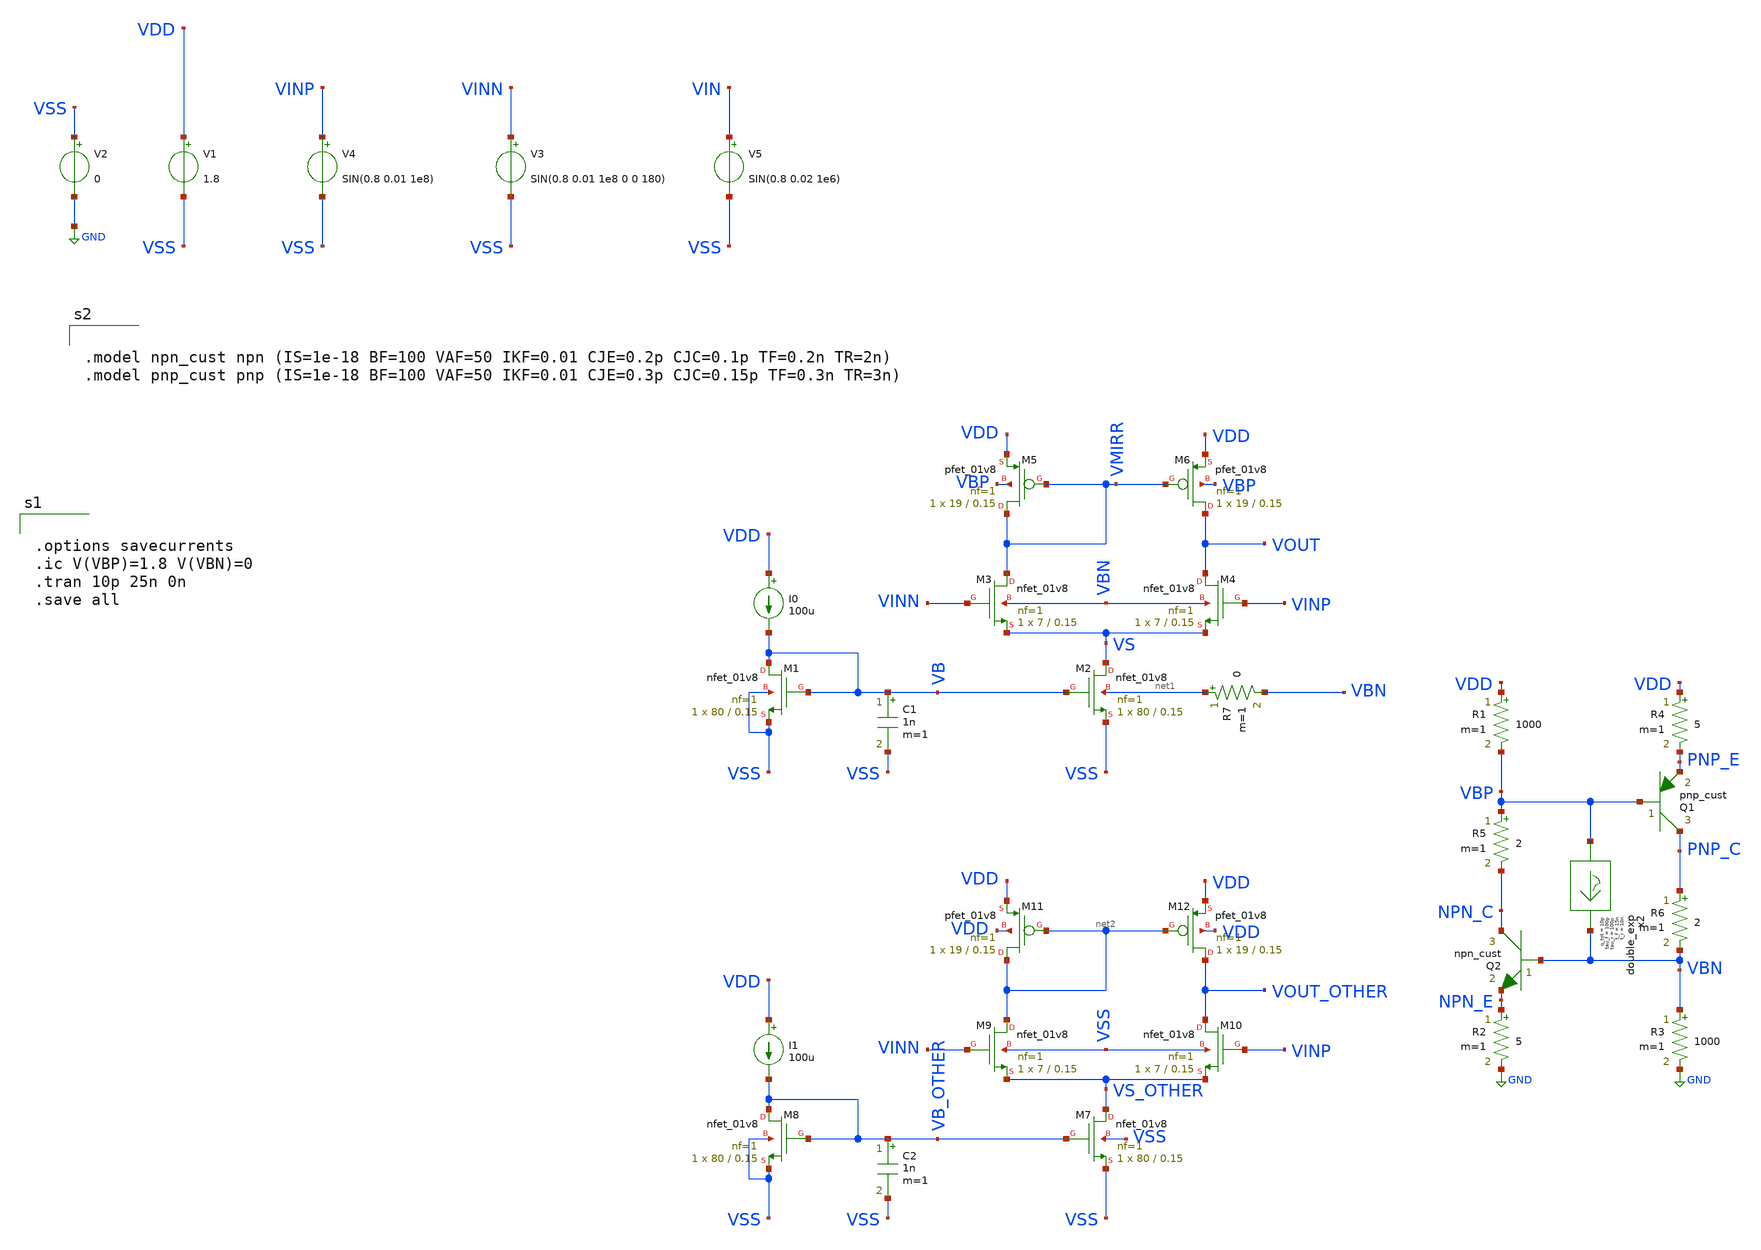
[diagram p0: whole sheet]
** sch_path: latchup/op_amp_test_intermed.sch
**.subckt op_amp_test_intermed
XM2 VS VB VSS net1 sky130_fd_pr__nfet_01v8 L=0.15 W=80 nf=1 ad='int((nf+1)/2) * W/nf * 0.29' as='int((nf+2)/2) * W/nf * 0.29'
+ pd='2*int((nf+1)/2) * (W/nf + 0.29)' ps='2*int((nf+2)/2) * (W/nf + 0.29)' nrd='0.29 / W' nrs='0.29 / W'
+ sa=0 sb=0 sd=0 mult=1 m=1
V1 VDD VSS 1.8
V2 VSS GND 0
XM1 VB VB VSS VSS sky130_fd_pr__nfet_01v8 L=0.15 W=80 nf=1 ad='int((nf+1)/2) * W/nf * 0.29' as='int((nf+2)/2) * W/nf * 0.29'
+ pd='2*int((nf+1)/2) * (W/nf + 0.29)' ps='2*int((nf+2)/2) * (W/nf + 0.29)' nrd='0.29 / W' nrs='0.29 / W'
+ sa=0 sb=0 sd=0 mult=1 m=1
I0 VDD VB 100u
XM3 VMIRR VINN VS VBN sky130_fd_pr__nfet_01v8 L=0.15 W=7 nf=1 ad='int((nf+1)/2) * W/nf * 0.29' as='int((nf+2)/2) * W/nf * 0.29'
+ pd='2*int((nf+1)/2) * (W/nf + 0.29)' ps='2*int((nf+2)/2) * (W/nf + 0.29)' nrd='0.29 / W' nrs='0.29 / W'
+ sa=0 sb=0 sd=0 mult=1 m=1
XM4 VOUT VINP VS VBN sky130_fd_pr__nfet_01v8 L=0.15 W=7 nf=1 ad='int((nf+1)/2) * W/nf * 0.29' as='int((nf+2)/2) * W/nf * 0.29'
+ pd='2*int((nf+1)/2) * (W/nf + 0.29)' ps='2*int((nf+2)/2) * (W/nf + 0.29)' nrd='0.29 / W' nrs='0.29 / W'
+ sa=0 sb=0 sd=0 mult=1 m=1
XM5 VMIRR VMIRR VDD VBP sky130_fd_pr__pfet_01v8 L=0.15 W=19 nf=1 ad='int((nf+1)/2) * W/nf * 0.29' as='int((nf+2)/2) * W/nf * 0.29'
+ pd='2*int((nf+1)/2) * (W/nf + 0.29)' ps='2*int((nf+2)/2) * (W/nf + 0.29)' nrd='0.29 / W' nrs='0.29 / W'
+ sa=0 sb=0 sd=0 mult=1 m=1
XM6 VOUT VMIRR VDD VBP sky130_fd_pr__pfet_01v8 L=0.15 W=19 nf=1 ad='int((nf+1)/2) * W/nf * 0.29' as='int((nf+2)/2) * W/nf * 0.29'
+ pd='2*int((nf+1)/2) * (W/nf + 0.29)' ps='2*int((nf+2)/2) * (W/nf + 0.29)' nrd='0.29 / W' nrs='0.29 / W'
+ sa=0 sb=0 sd=0 mult=1 m=1
V4 VINP VSS SIN(0.8 0.01 1e8)
V3 VINN VSS SIN(0.8 0.01 1e8 0 0 180)
C1 VB VSS 1n m=1
V5 VIN VSS SIN(0.8 0.02 1e6)
XM7 VS_OTHER VB_OTHER VSS VSS sky130_fd_pr__nfet_01v8 L=0.15 W=80 nf=1 ad='int((nf+1)/2) * W/nf * 0.29'
+ as='int((nf+2)/2) * W/nf * 0.29' pd='2*int((nf+1)/2) * (W/nf + 0.29)' ps='2*int((nf+2)/2) * (W/nf + 0.29)'
+ nrd='0.29 / W' nrs='0.29 / W' sa=0 sb=0 sd=0 mult=1 m=1
XM8 VB_OTHER VB_OTHER VSS VSS sky130_fd_pr__nfet_01v8 L=0.15 W=80 nf=1 ad='int((nf+1)/2) * W/nf * 0.29'
+ as='int((nf+2)/2) * W/nf * 0.29' pd='2*int((nf+1)/2) * (W/nf + 0.29)' ps='2*int((nf+2)/2) * (W/nf + 0.29)'
+ nrd='0.29 / W' nrs='0.29 / W' sa=0 sb=0 sd=0 mult=1 m=1
I1 VDD VB_OTHER 100u
XM9 net2 VINN VS_OTHER VSS sky130_fd_pr__nfet_01v8 L=0.15 W=7 nf=1 ad='int((nf+1)/2) * W/nf * 0.29' as='int((nf+2)/2) * W/nf * 0.29'
+ pd='2*int((nf+1)/2) * (W/nf + 0.29)' ps='2*int((nf+2)/2) * (W/nf + 0.29)' nrd='0.29 / W' nrs='0.29 / W'
+ sa=0 sb=0 sd=0 mult=1 m=1
XM10 VOUT_OTHER VINP VS_OTHER VSS sky130_fd_pr__nfet_01v8 L=0.15 W=7 nf=1 ad='int((nf+1)/2) * W/nf * 0.29'
+ as='int((nf+2)/2) * W/nf * 0.29' pd='2*int((nf+1)/2) * (W/nf + 0.29)' ps='2*int((nf+2)/2) * (W/nf + 0.29)'
+ nrd='0.29 / W' nrs='0.29 / W' sa=0 sb=0 sd=0 mult=1 m=1
XM11 net2 net2 VDD VDD sky130_fd_pr__pfet_01v8 L=0.15 W=19 nf=1 ad='int((nf+1)/2) * W/nf * 0.29' as='int((nf+2)/2) * W/nf * 0.29'
+ pd='2*int((nf+1)/2) * (W/nf + 0.29)' ps='2*int((nf+2)/2) * (W/nf + 0.29)' nrd='0.29 / W' nrs='0.29 / W'
+ sa=0 sb=0 sd=0 mult=1 m=1
XM12 VOUT_OTHER net2 VDD VDD sky130_fd_pr__pfet_01v8 L=0.15 W=19 nf=1 ad='int((nf+1)/2) * W/nf * 0.29'
+ as='int((nf+2)/2) * W/nf * 0.29' pd='2*int((nf+1)/2) * (W/nf + 0.29)' ps='2*int((nf+2)/2) * (W/nf + 0.29)'
+ nrd='0.29 / W' nrs='0.29 / W' sa=0 sb=0 sd=0 mult=1 m=1
C2 VB_OTHER VSS 1n m=1
Q1 PNP_C VBP PNP_E pnp_cust area=1 m=1
Q2 NPN_C VBN NPN_E npn_cust area=1 m=1
R3 VBN GND 1000 m=1
R4 VDD PNP_E 5 m=1
R1 VDD VBP 1000 m=1
R2 NPN_E GND 5 m=1
R5 VBP NPN_C 2 m=1
R6 PNP_C VBN 2 m=1
x2 VBP VBN double_exp t_r=10n tau_r=100p t_f=15n tau_f=100p q_tot=10p
R7 net1 VBN 0 m=1
**** begin user architecture code


.options savecurrents
.ic V(VBP)=1.8 V(VBN)=0
.tran 10p 25n 0n
.save all



** opencircuitdesign pdks install
.lib $::SKYWATER_MODELS/sky130.lib.spice tt




.include /usr/local/share/rad_modeling_blocks/rad_modeling_blocks.spice




.model npn_cust npn (IS=1e-18 BF=100 VAF=50 IKF=0.01 CJE=0.2p CJC=0.1p TF=0.2n TR=2n)
.model pnp_cust pnp (IS=1e-18 BF=100 VAF=50 IKF=0.01 CJE=0.3p CJC=0.15p TF=0.3n TR=3n)


**** end user architecture code
**.ends

* expanding   symbol:  double_exp.sym # of pins=2
** sym_path: xschem_rad_library/double_exp.sym
** sch_path: xschem_rad_library/double_exp.sch
.subckt double_exp in out  t_r=0 t_f=0 tau_r=0 tau_f=0 q_tot=0
*.opin OUT
*.ipin IN
I1 IN OUT EXP(0 {q_tot / (t_f-t_r+tau_f-tau_r)} {t_r} {tau_r} {t_f} {tau_f})
.ends

.GLOBAL GND
.end
